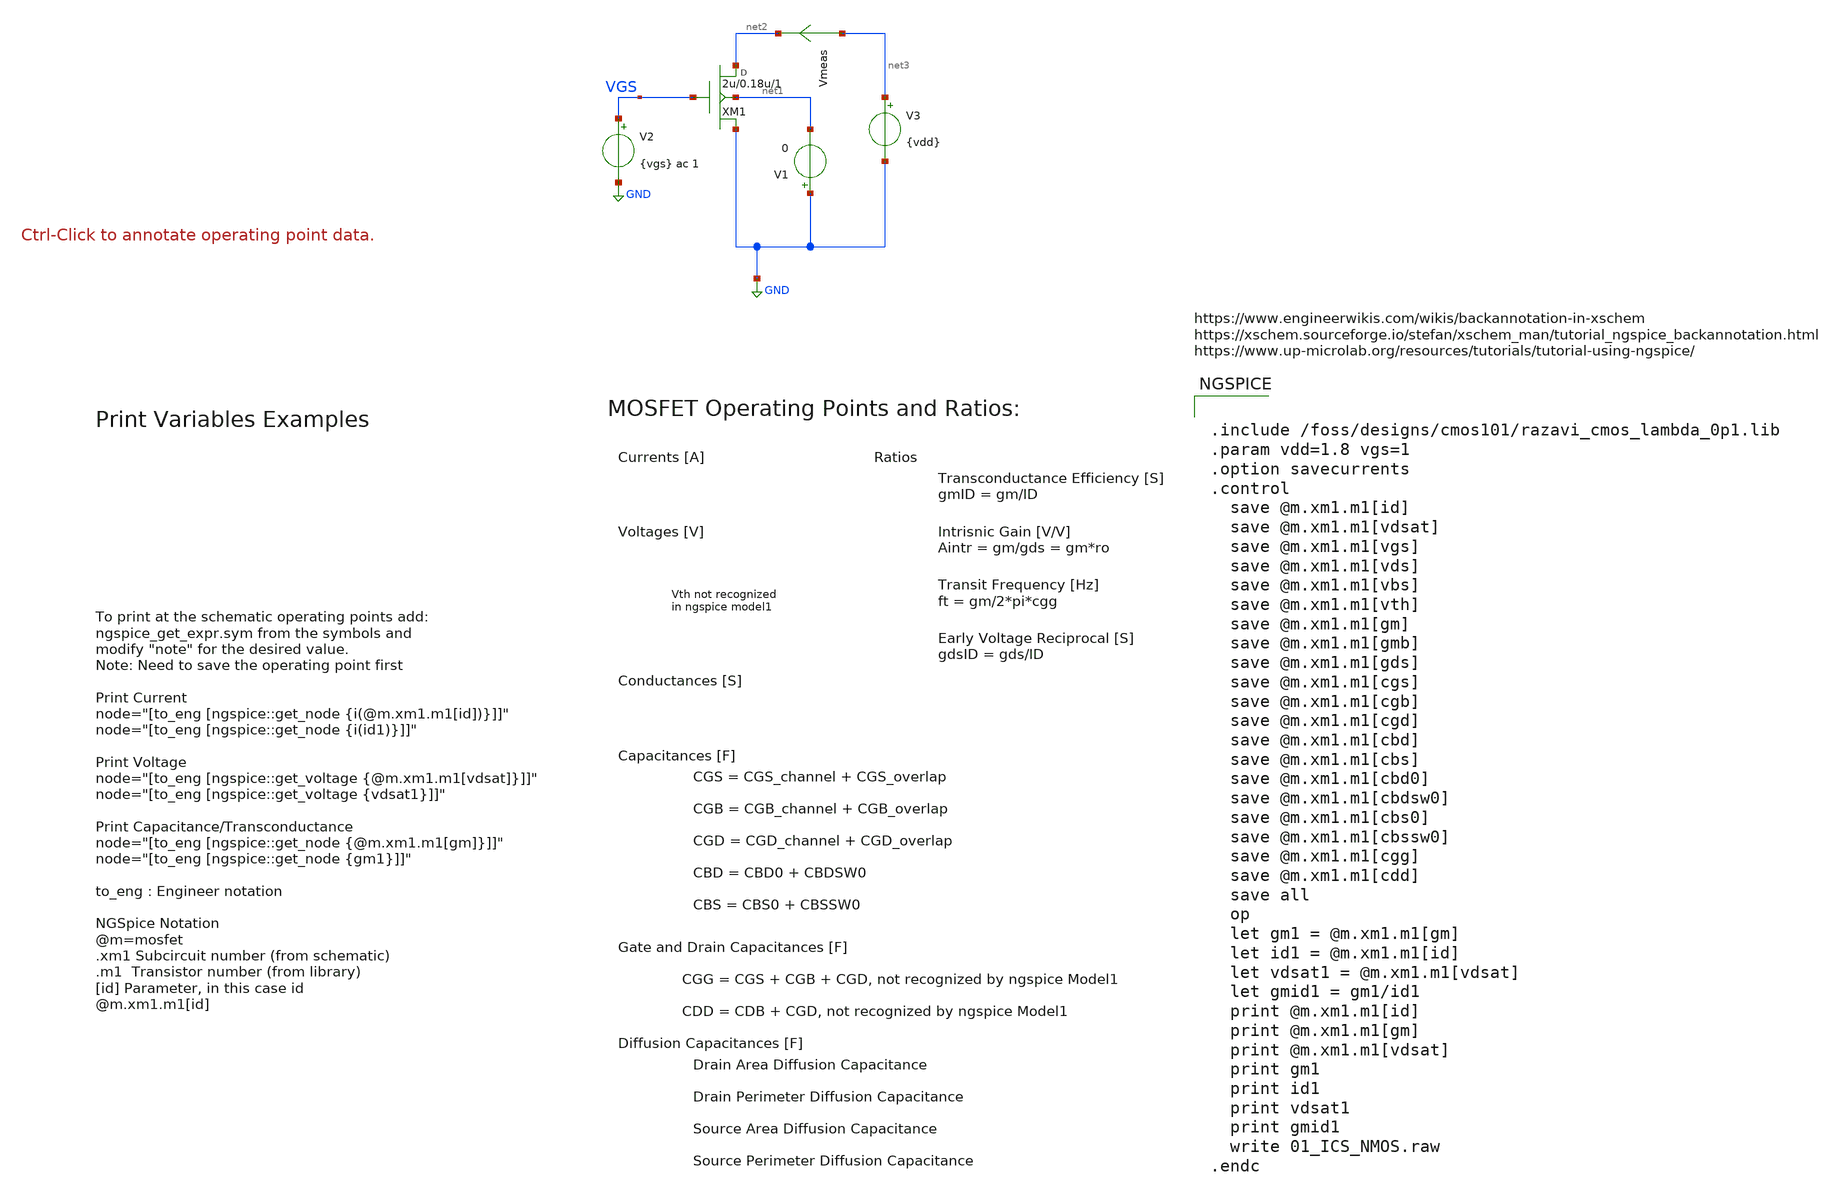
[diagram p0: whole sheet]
** sch_path: Xschem/gf180mcuD/gmID_Designs/01_ICS_NMOS.sch
**.subckt 01_ICS_NMOS
XM1 net2 VGS GND net1 xnch w=2u l=0.18u m=1
V1 GND net1 0
Vmeas net3 net2 0
.save i(vmeas)
V2 VGS GND {vgs} ac 1
V3 net3 GND {vdd}
**** begin user architecture code


.include /foss/designs/cmos101/razavi_cmos_lambda_0p1.lib
.param vdd=1.8 vgs=1
.option savecurrents
.control
  save @m.xm1.m1[id]
  save @m.xm1.m1[vdsat]
  save @m.xm1.m1[vgs]
  save @m.xm1.m1[vds]
  save @m.xm1.m1[vbs]
  save @m.xm1.m1[vth]
  save @m.xm1.m1[gm]
  save @m.xm1.m1[gmb]
  save @m.xm1.m1[gds]
  save @m.xm1.m1[cgs]
  save @m.xm1.m1[cgb]
  save @m.xm1.m1[cgd]
  save @m.xm1.m1[cbd]
  save @m.xm1.m1[cbs]
  save @m.xm1.m1[cbd0]
  save @m.xm1.m1[cbdsw0]
  save @m.xm1.m1[cbs0]
  save @m.xm1.m1[cbssw0]
  save @m.xm1.m1[cgg]
  save @m.xm1.m1[cdd]
  save all
  op
  let gm1 = @m.xm1.m1[gm]
  let id1 = @m.xm1.m1[id]
  let vdsat1 = @m.xm1.m1[vdsat]
  let gmid1 = gm1/id1
  print @m.xm1.m1[id]
  print @m.xm1.m1[gm]
  print @m.xm1.m1[vdsat]
  print gm1
  print id1
  print vdsat1
  print gmid1
  write 01_ICS_NMOS.raw
.endc


**** end user architecture code
**.ends
.GLOBAL GND
.end
